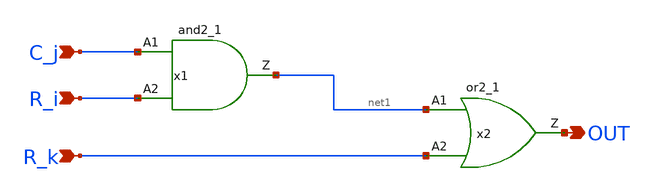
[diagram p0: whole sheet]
** sch_path: DAC/xschem/digital_cell/dac_local_decoder.sch
**.subckt dac_local_decoder C_j R_k R_i OUT
*.ipin C_j
*.ipin R_k
*.ipin R_i
*.opin OUT
x1 C_j R_i net1 VDD VNW VPW VSS gf180mcu_fd_sc_mcu7t5v0__and2_1
x2 net1 R_k OUT VDD VNW VPW VSS gf180mcu_fd_sc_mcu7t5v0__or2_1
**.ends
.end
